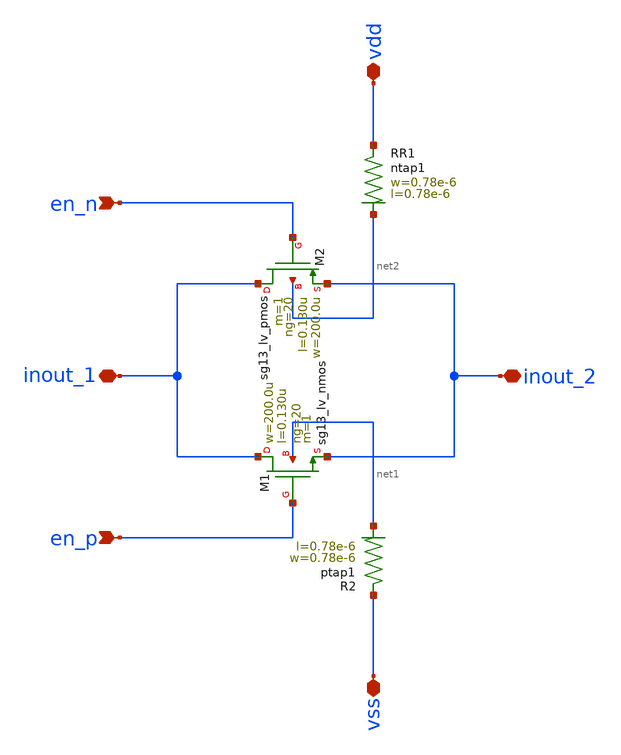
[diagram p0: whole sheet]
** sch_path: CHIPCHILE_CANELOS24_WorkshopTO/design_data/xschem/multiplexer/transmission_gate.sch
**.subckt transmission_gate inout_1 inout_2 en_p vdd vss en_n
*.iopin inout_1
*.iopin inout_2
*.ipin en_p
*.iopin vdd
*.iopin vss
*.ipin en_n
XM1 inout_1 en_p inout_2 net1 sg13_lv_nmos w=200.0u l=0.130u ng=20 m=1 mm_ok=1
XM2 inout_1 en_n inout_2 net2 sg13_lv_pmos w=200.0u l=0.130u ng=20 m=1 mm_ok=1
XR1 vdd net2 ntap1 R=262.8 w=0.78e-6 l=0.78e-6
XR2 vss net1 ptap1 R=262.8 w=0.78e-6 l=0.78e-6
**.ends
.end
